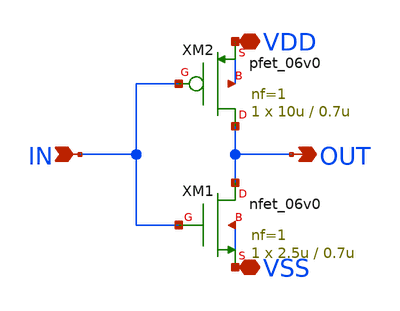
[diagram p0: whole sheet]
** sch_path: inverters/inverter_v4.sch
**.subckt inverter_v4 IN OUT VDD VSS
*.ipin IN
*.opin OUT
*.iopin VDD
*.iopin VSS
XM1 OUT IN VSS VSS nfet_06v0 L=0.7u W=2.5u nf=1 ad='int((nf+1)/2) * W/nf * 0.18u' as='int((nf+2)/2) * W/nf * 0.18u'
+ pd='2*int((nf+1)/2) * (W/nf + 0.18u)' ps='2*int((nf+2)/2) * (W/nf + 0.18u)' nrd='0.18u / W' nrs='0.18u / W'
+ sa=0 sb=0 sd=0 m=1
XM2 OUT IN VDD VDD pfet_06v0 L=0.7u W=10u nf=1 ad='int((nf+1)/2) * W/nf * 0.18u' as='int((nf+2)/2) * W/nf * 0.18u'
+ pd='2*int((nf+1)/2) * (W/nf + 0.18u)' ps='2*int((nf+2)/2) * (W/nf + 0.18u)' nrd='0.18u / W' nrs='0.18u / W'
+ sa=0 sb=0 sd=0 m=1
**.ends
.end
